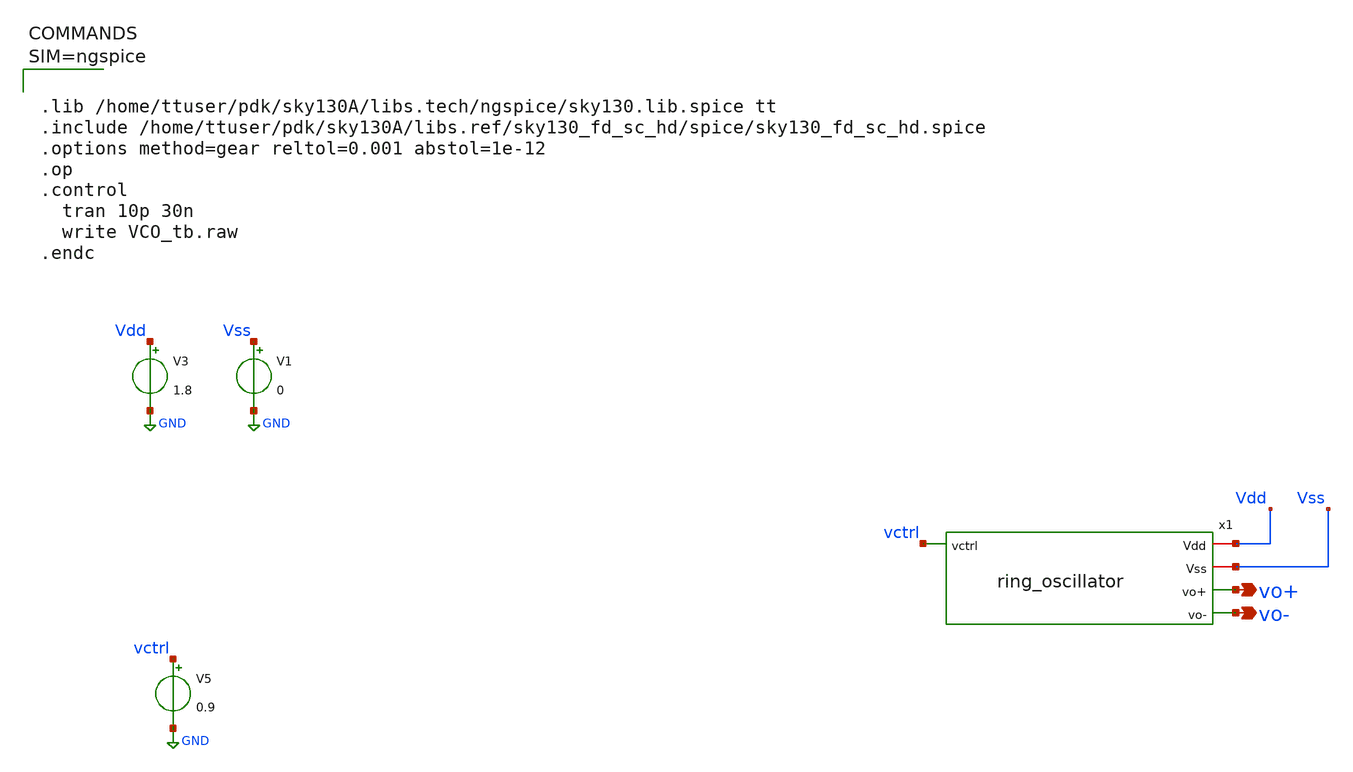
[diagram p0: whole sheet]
** sch_path: xschem/ring_oscillator_tb.sch
**.subckt ring_oscillator_tb vo+ vo-
*.opin vo+
*.opin vo-
V3 Vdd GND 1.8
V1 Vss GND 0
V5 vctrl GND 0.9
x1 Vdd Vss vctrl vo+ vo- ring_oscillator
**** begin user architecture code



.lib /home/ttuser/pdk/sky130A/libs.tech/ngspice/sky130.lib.spice tt
.include /home/ttuser/pdk/sky130A/libs.ref/sky130_fd_sc_hd/spice/sky130_fd_sc_hd.spice
.options method=gear reltol=0.001 abstol=1e-12
.op
.control
  tran 10p 30n
  write VCO_tb.raw
.endc



**** end user architecture code
**.ends
.GLOBAL GND
.end
